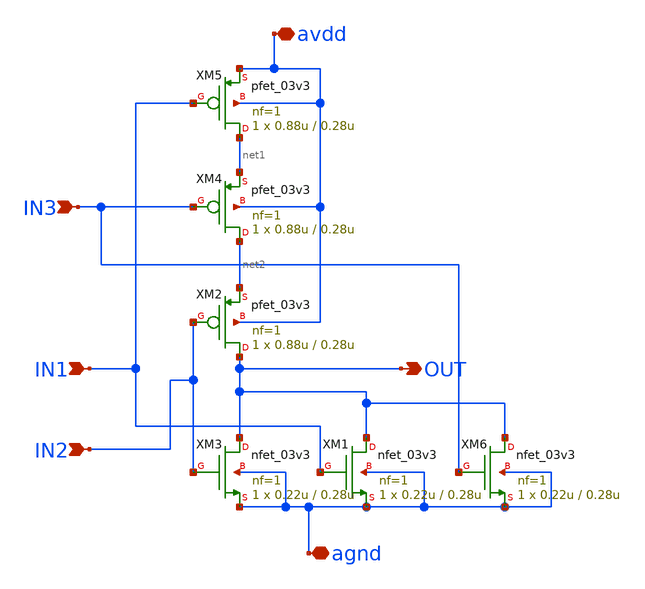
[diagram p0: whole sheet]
** sch_path: mpw18h1/cisar-gen/xschem/TBD/nor3.sch
**.subckt nor3 OUT IN1 IN2 avdd agnd IN3
*.opin OUT
*.ipin IN1
*.ipin IN2
*.iopin avdd
*.iopin agnd
*.ipin IN3
XM2 OUT IN2 net2 avdd pfet_03v3 L=0.28u W=0.88u nf=1 ad='int((nf+1)/2) * W/nf * 0.18u' as='int((nf+2)/2) * W/nf * 0.18u'
+ pd='2*int((nf+1)/2) * (W/nf + 0.18u)' ps='2*int((nf+2)/2) * (W/nf + 0.18u)' nrd='0.18u / W' nrs='0.18u / W'
+ sa=0 sb=0 sd=0 m=1
XM5 net1 IN1 avdd avdd pfet_03v3 L=0.28u W=0.88u nf=1 ad='int((nf+1)/2) * W/nf * 0.18u' as='int((nf+2)/2) * W/nf * 0.18u'
+ pd='2*int((nf+1)/2) * (W/nf + 0.18u)' ps='2*int((nf+2)/2) * (W/nf + 0.18u)' nrd='0.18u / W' nrs='0.18u / W'
+ sa=0 sb=0 sd=0 m=1
XM1 OUT IN1 agnd agnd nfet_03v3 L=0.28u W=0.22u nf=1 ad='int((nf+1)/2) * W/nf * 0.18u' as='int((nf+2)/2) * W/nf * 0.18u'
+ pd='2*int((nf+1)/2) * (W/nf + 0.18u)' ps='2*int((nf+2)/2) * (W/nf + 0.18u)' nrd='0.18u / W' nrs='0.18u / W'
+ sa=0 sb=0 sd=0 m=1
XM3 OUT IN2 agnd agnd nfet_03v3 L=0.28u W=0.22u nf=1 ad='int((nf+1)/2) * W/nf * 0.18u' as='int((nf+2)/2) * W/nf * 0.18u'
+ pd='2*int((nf+1)/2) * (W/nf + 0.18u)' ps='2*int((nf+2)/2) * (W/nf + 0.18u)' nrd='0.18u / W' nrs='0.18u / W'
+ sa=0 sb=0 sd=0 m=1
XM4 net2 IN3 net1 avdd pfet_03v3 L=0.28u W=0.88u nf=1 ad='int((nf+1)/2) * W/nf * 0.18u' as='int((nf+2)/2) * W/nf * 0.18u'
+ pd='2*int((nf+1)/2) * (W/nf + 0.18u)' ps='2*int((nf+2)/2) * (W/nf + 0.18u)' nrd='0.18u / W' nrs='0.18u / W'
+ sa=0 sb=0 sd=0 m=1
XM6 OUT IN3 agnd agnd nfet_03v3 L=0.28u W=0.22u nf=1 ad='int((nf+1)/2) * W/nf * 0.18u' as='int((nf+2)/2) * W/nf * 0.18u'
+ pd='2*int((nf+1)/2) * (W/nf + 0.18u)' ps='2*int((nf+2)/2) * (W/nf + 0.18u)' nrd='0.18u / W' nrs='0.18u / W'
+ sa=0 sb=0 sd=0 m=1
**.ends
.end
